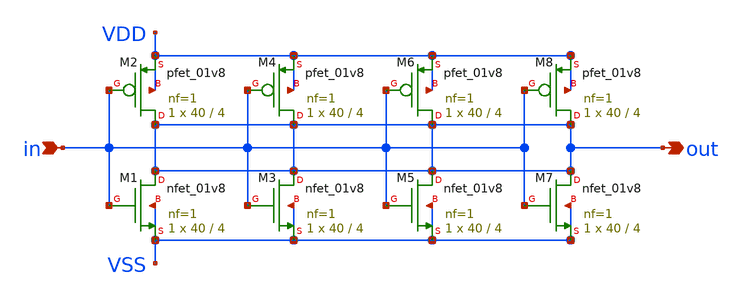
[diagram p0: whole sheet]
** sch_path: tt_um_wulf_8bit_vco/xschem/lib/buf_drv.sch
**.subckt buf_drv out in
*.opin out
*.ipin in
XM1 out in VSS VSS sky130_fd_pr__nfet_01v8 L=4 W=40 nf=1 ad='int((1 + 1)/2) * 40 / 1 * 0.29' as='int((1 + 2)/2) * 40 / 1 * 0.29'
+ pd='2*int((1 + 1)/2) * (40 / 1 + 0.29)' ps='2*int((1 + 2)/2) * (40 / 1 + 0.29)' nrd='0.29 / 40 ' nrs='0.29 / 40 '
+ sa=0 sb=0 sd=0 mult=1 m=1
XM2 out in VDD VDD sky130_fd_pr__pfet_01v8 L=4 W=40 nf=1 ad='int((nf+1)/2) * W/nf * 0.29' as='int((nf+2)/2) * W/nf * 0.29'
+ pd='2*int((nf+1)/2) * (W/nf + 0.29)' ps='2*int((nf+2)/2) * (W/nf + 0.29)' nrd='0.29 / W' nrs='0.29 / W'
+ sa=0 sb=0 sd=0 mult=1 m=1
XM3 out in VSS VSS sky130_fd_pr__nfet_01v8 L=4 W=40 nf=1 ad='int((1 + 1)/2) * 40 / 1 * 0.29' as='int((1 + 2)/2) * 40 / 1 * 0.29'
+ pd='2*int((1 + 1)/2) * (40 / 1 + 0.29)' ps='2*int((1 + 2)/2) * (40 / 1 + 0.29)' nrd='0.29 / 40 ' nrs='0.29 / 40 '
+ sa=0 sb=0 sd=0 mult=1 m=1
XM5 out in VSS VSS sky130_fd_pr__nfet_01v8 L=4 W=40 nf=1 ad='int((1 + 1)/2) * 40 / 1 * 0.29' as='int((1 + 2)/2) * 40 / 1 * 0.29'
+ pd='2*int((1 + 1)/2) * (40 / 1 + 0.29)' ps='2*int((1 + 2)/2) * (40 / 1 + 0.29)' nrd='0.29 / 40 ' nrs='0.29 / 40 '
+ sa=0 sb=0 sd=0 mult=1 m=1
XM7 out in VSS VSS sky130_fd_pr__nfet_01v8 L=4 W=40 nf=1 ad='int((1 + 1)/2) * 40 / 1 * 0.29' as='int((1 + 2)/2) * 40 / 1 * 0.29'
+ pd='2*int((1 + 1)/2) * (40 / 1 + 0.29)' ps='2*int((1 + 2)/2) * (40 / 1 + 0.29)' nrd='0.29 / 40 ' nrs='0.29 / 40 '
+ sa=0 sb=0 sd=0 mult=1 m=1
XM4 out in VDD VDD sky130_fd_pr__pfet_01v8 L=4 W=40 nf=1 ad='int((nf+1)/2) * W/nf * 0.29' as='int((nf+2)/2) * W/nf * 0.29'
+ pd='2*int((nf+1)/2) * (W/nf + 0.29)' ps='2*int((nf+2)/2) * (W/nf + 0.29)' nrd='0.29 / W' nrs='0.29 / W'
+ sa=0 sb=0 sd=0 mult=1 m=1
XM6 out in VDD VDD sky130_fd_pr__pfet_01v8 L=4 W=40 nf=1 ad='int((nf+1)/2) * W/nf * 0.29' as='int((nf+2)/2) * W/nf * 0.29'
+ pd='2*int((nf+1)/2) * (W/nf + 0.29)' ps='2*int((nf+2)/2) * (W/nf + 0.29)' nrd='0.29 / W' nrs='0.29 / W'
+ sa=0 sb=0 sd=0 mult=1 m=1
XM8 out in VDD VDD sky130_fd_pr__pfet_01v8 L=4 W=40 nf=1 ad='int((nf+1)/2) * W/nf * 0.29' as='int((nf+2)/2) * W/nf * 0.29'
+ pd='2*int((nf+1)/2) * (W/nf + 0.29)' ps='2*int((nf+2)/2) * (W/nf + 0.29)' nrd='0.29 / W' nrs='0.29 / W'
+ sa=0 sb=0 sd=0 mult=1 m=1
**.ends
.end
